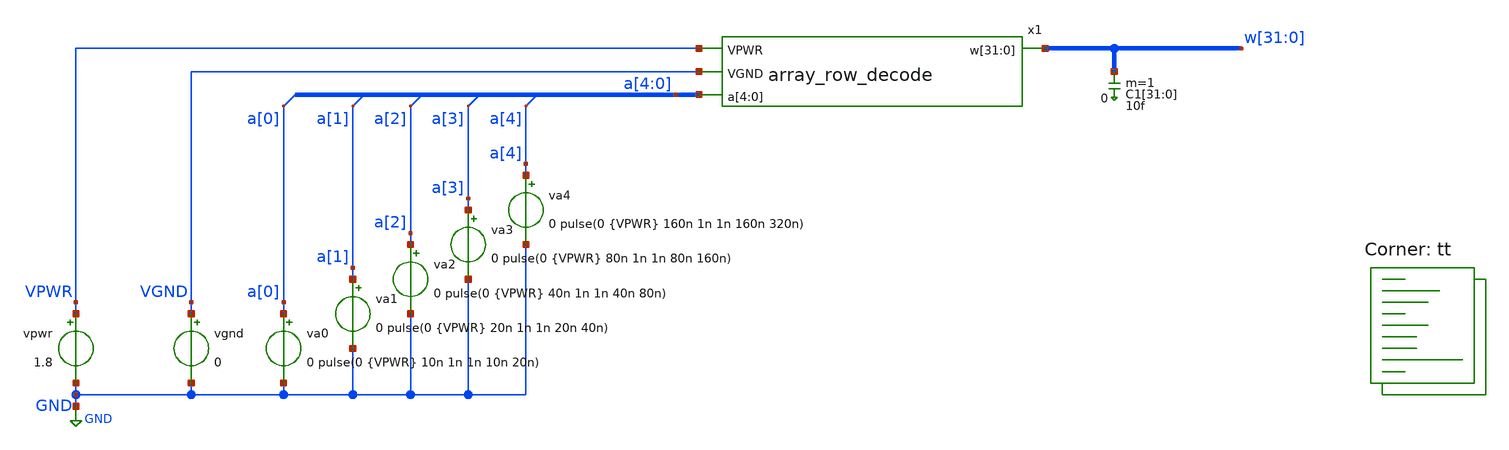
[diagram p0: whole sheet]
** sch_path: xschem/test_array_row_decode.sch
**.subckt test_array_row_decode
x1 VPWR VGND a[4] a[3] a[2] a[1] a[0] w[31] w[30] w[29] w[28] w[27] w[26] w[25] w[24] w[23] w[22]
+ w[21] w[20] w[19] w[18] w[17] w[16] w[15] w[14] w[13] w[12] w[11] w[10] w[9] w[8] w[7] w[6] w[5] w[4]
+ w[3] w[2] w[1] w[0] array_row_decode
vpwr VPWR GND 1.8
va0 a[0] GND 0 pulse(0 {VPWR} 10n 1n 1n 10n 20n)
vgnd VGND GND 0
va1 a[1] GND 0 pulse(0 {VPWR} 20n 1n 1n 20n 40n)
va2 a[2] GND 0 pulse(0 {VPWR} 40n 1n 1n 40n 80n)
va3 a[3] GND 0 pulse(0 {VPWR} 80n 1n 1n 80n 160n)
va4 a[4] GND 0 pulse(0 {VPWR} 160n 1n 1n 160n 320n)
C1[31] w[31] 0 10f m=1
C1[30] w[30] 0 10f m=1
C1[29] w[29] 0 10f m=1
C1[28] w[28] 0 10f m=1
C1[27] w[27] 0 10f m=1
C1[26] w[26] 0 10f m=1
C1[25] w[25] 0 10f m=1
C1[24] w[24] 0 10f m=1
C1[23] w[23] 0 10f m=1
C1[22] w[22] 0 10f m=1
C1[21] w[21] 0 10f m=1
C1[20] w[20] 0 10f m=1
C1[19] w[19] 0 10f m=1
C1[18] w[18] 0 10f m=1
C1[17] w[17] 0 10f m=1
C1[16] w[16] 0 10f m=1
C1[15] w[15] 0 10f m=1
C1[14] w[14] 0 10f m=1
C1[13] w[13] 0 10f m=1
C1[12] w[12] 0 10f m=1
C1[11] w[11] 0 10f m=1
C1[10] w[10] 0 10f m=1
C1[9] w[9] 0 10f m=1
C1[8] w[8] 0 10f m=1
C1[7] w[7] 0 10f m=1
C1[6] w[6] 0 10f m=1
C1[5] w[5] 0 10f m=1
C1[4] w[4] 0 10f m=1
C1[3] w[3] 0 10f m=1
C1[2] w[2] 0 10f m=1
C1[1] w[1] 0 10f m=1
C1[0] w[0] 0 10f m=1
**** begin user architecture code
.lib $::SKYWATER_MODELS/sky130.lib.spice tt



.param VPWR=1.8
.param VSS=0
.options savecurrents
.control
  save all
  op
  remzerovec
  write test_array_row_decode.raw
  set appendwrite
  * tran
  tran 1n 1u
  remzerovec
  write test_array_row_decode.raw
.endc



**** end user architecture code
**.ends

* expanding   symbol:  array_row_decode.sym # of pins=4
** sym_path: xschem/array_row_decode.sym
** sch_path: xschem/array_row_decode.sch
.subckt array_row_decode VPWR VGND a[4] a[3] a[2] a[1] a[0] w[31] w[30] w[29] w[28] w[27] w[26]
+ w[25] w[24] w[23] w[22] w[21] w[20] w[19] w[18] w[17] w[16] w[15] w[14] w[13] w[12] w[11] w[10] w[9] w[8]
+ w[7] w[6] w[5] w[4] w[3] w[2] w[1] w[0]
*.ipin a[4],a[3],a[2],a[1],a[0]
*.ipin VPWR
*.ipin VGND
*.opin
*+ w[31],w[30],w[29],w[28],w[27],w[26],w[25],w[24],w[23],w[22],w[21],w[20],w[19],w[18],w[17],w[16],w[15],w[14],w[13],w[12],w[11],w[10],w[9],w[8],w[7],w[6],w[5],w[4],w[3],w[2],w[1],w[0]
x1 a[4] VGND VGND VPWR VPWR a[4]_b sky130_fd_sc_hd__inv_1
x2 a[3] VGND VGND VPWR VPWR a[3]_b sky130_fd_sc_hd__inv_1
x3 a[2] VGND VGND VPWR VPWR a[2]_b sky130_fd_sc_hd__inv_1
x4 a[1] VGND VGND VPWR VPWR a[1]_b sky130_fd_sc_hd__inv_1
x5 a[0] VGND VGND VPWR VPWR a[0]_b sky130_fd_sc_hd__inv_1
x13 a[2] a[3] VGND VGND VPWR VPWR net8 sky130_fd_sc_hd__nand2_2
x6 a[0]_b a[1]_b VGND VGND VPWR VPWR net1 sky130_fd_sc_hd__nand2_2
x7 a[0] a[1]_b VGND VGND VPWR VPWR net3 sky130_fd_sc_hd__nand2_2
x8 a[0]_b a[1] VGND VGND VPWR VPWR net4 sky130_fd_sc_hd__nand2_2
x9 a[0] a[1] VGND VGND VPWR VPWR net5 sky130_fd_sc_hd__nand2_2
x10 a[2]_b a[3]_b VGND VGND VPWR VPWR net2 sky130_fd_sc_hd__nand2_2
x11 a[2] a[3]_b VGND VGND VPWR VPWR net6 sky130_fd_sc_hd__nand2_2
x12 a[2]_b a[3] VGND VGND VPWR VPWR net7 sky130_fd_sc_hd__nand2_2
x14 net1 net2 a[4] VGND VGND VPWR VPWR w[0] sky130_fd_sc_hd__nor3_1
x15 net3 net2 a[4] VGND VGND VPWR VPWR w[1] sky130_fd_sc_hd__nor3_1
x16 net4 net2 a[4] VGND VGND VPWR VPWR w[2] sky130_fd_sc_hd__nor3_1
x17 net5 net2 a[4] VGND VGND VPWR VPWR w[3] sky130_fd_sc_hd__nor3_1
x18 net1 net6 a[4] VGND VGND VPWR VPWR w[4] sky130_fd_sc_hd__nor3_1
x19 net3 net6 a[4] VGND VGND VPWR VPWR w[5] sky130_fd_sc_hd__nor3_1
x20 net4 net6 a[4] VGND VGND VPWR VPWR w[6] sky130_fd_sc_hd__nor3_1
x21 net5 net6 a[4] VGND VGND VPWR VPWR w[7] sky130_fd_sc_hd__nor3_1
x22 net1 net7 a[4] VGND VGND VPWR VPWR w[8] sky130_fd_sc_hd__nor3_1
x23 net3 net7 a[4] VGND VGND VPWR VPWR w[9] sky130_fd_sc_hd__nor3_1
x24 net4 net7 a[4] VGND VGND VPWR VPWR w[10] sky130_fd_sc_hd__nor3_1
x25 net5 net7 a[4] VGND VGND VPWR VPWR w[11] sky130_fd_sc_hd__nor3_1
x26 net1 net8 a[4] VGND VGND VPWR VPWR w[12] sky130_fd_sc_hd__nor3_1
x27 net3 net8 a[4] VGND VGND VPWR VPWR w[13] sky130_fd_sc_hd__nor3_1
x28 net4 net8 a[4] VGND VGND VPWR VPWR w[14] sky130_fd_sc_hd__nor3_1
x29 net5 net8 a[4] VGND VGND VPWR VPWR w[15] sky130_fd_sc_hd__nor3_1
x30 net1 net2 a[4]_b VGND VGND VPWR VPWR w[16] sky130_fd_sc_hd__nor3_1
x31 net3 net2 a[4]_b VGND VGND VPWR VPWR w[17] sky130_fd_sc_hd__nor3_1
x32 net4 net2 a[4]_b VGND VGND VPWR VPWR w[18] sky130_fd_sc_hd__nor3_1
x33 net5 net2 a[4]_b VGND VGND VPWR VPWR w[19] sky130_fd_sc_hd__nor3_1
x34 net1 net6 a[4]_b VGND VGND VPWR VPWR w[20] sky130_fd_sc_hd__nor3_1
x35 net3 net6 a[4]_b VGND VGND VPWR VPWR w[21] sky130_fd_sc_hd__nor3_1
x36 net4 net6 a[4]_b VGND VGND VPWR VPWR w[22] sky130_fd_sc_hd__nor3_1
x37 net5 net6 a[4]_b VGND VGND VPWR VPWR w[23] sky130_fd_sc_hd__nor3_1
x38 net1 net7 a[4]_b VGND VGND VPWR VPWR w[24] sky130_fd_sc_hd__nor3_1
x39 net3 net7 a[4]_b VGND VGND VPWR VPWR w[25] sky130_fd_sc_hd__nor3_1
x40 net4 net7 a[4]_b VGND VGND VPWR VPWR w[26] sky130_fd_sc_hd__nor3_1
x41 net5 net7 a[4]_b VGND VGND VPWR VPWR w[27] sky130_fd_sc_hd__nor3_1
x42 net1 net8 a[4]_b VGND VGND VPWR VPWR w[28] sky130_fd_sc_hd__nor3_1
x43 net3 net8 a[4]_b VGND VGND VPWR VPWR w[29] sky130_fd_sc_hd__nor3_1
x44 net4 net8 a[4]_b VGND VGND VPWR VPWR w[30] sky130_fd_sc_hd__nor3_1
x45 net5 net8 a[4]_b VGND VGND VPWR VPWR w[31] sky130_fd_sc_hd__nor3_1
x46 VGND VPWR sky130_fd_sc_hd__tapvpwrvgnd_1
x47 VGND VGND VPWR VPWR sky130_fd_sc_hd__decap_3
x48 VGND VPWR sky130_fd_sc_hd__tapvpwrvgnd_1
x49 VGND VPWR sky130_fd_sc_hd__tapvpwrvgnd_1
x50 VGND VGND VPWR VPWR sky130_fd_sc_hd__decap_3
x51 VGND VPWR sky130_fd_sc_hd__tapvpwrvgnd_1
x52 VGND VPWR sky130_fd_sc_hd__tapvpwrvgnd_1
x53 VGND VGND VPWR VPWR sky130_fd_sc_hd__decap_3
x54 VGND VPWR sky130_fd_sc_hd__tapvpwrvgnd_1
x55 VGND VPWR sky130_fd_sc_hd__tapvpwrvgnd_1
x56 VGND VGND VPWR VPWR sky130_fd_sc_hd__decap_3
x57 VGND VPWR sky130_fd_sc_hd__tapvpwrvgnd_1
x58 VGND VPWR sky130_fd_sc_hd__tapvpwrvgnd_1
x59 VGND VGND VPWR VPWR sky130_fd_sc_hd__decap_3
x60 VGND VPWR sky130_fd_sc_hd__tapvpwrvgnd_1
x61 VGND VPWR sky130_fd_sc_hd__tapvpwrvgnd_1
x62 VGND VGND VPWR VPWR sky130_fd_sc_hd__decap_3
x63 VGND VPWR sky130_fd_sc_hd__tapvpwrvgnd_1
x64 VGND VPWR sky130_fd_sc_hd__tapvpwrvgnd_1
x65 VGND VGND VPWR VPWR sky130_fd_sc_hd__decap_3
x66 VGND VPWR sky130_fd_sc_hd__tapvpwrvgnd_1
x67 VGND VPWR sky130_fd_sc_hd__tapvpwrvgnd_1
x68 VGND VGND VPWR VPWR sky130_fd_sc_hd__decap_3
x69 VGND VPWR sky130_fd_sc_hd__tapvpwrvgnd_1
x70 VGND VPWR sky130_fd_sc_hd__tapvpwrvgnd_1
x71 VGND VGND VPWR VPWR sky130_fd_sc_hd__decap_3
x72 VGND VPWR sky130_fd_sc_hd__tapvpwrvgnd_1
x73 VGND VPWR sky130_fd_sc_hd__tapvpwrvgnd_1
x74 VGND VGND VPWR VPWR sky130_fd_sc_hd__decap_3
x75 VGND VPWR sky130_fd_sc_hd__tapvpwrvgnd_1
x76 VGND VPWR sky130_fd_sc_hd__tapvpwrvgnd_1
x77 VGND VGND VPWR VPWR sky130_fd_sc_hd__decap_3
x78 VGND VPWR sky130_fd_sc_hd__tapvpwrvgnd_1
x79 VGND VPWR sky130_fd_sc_hd__tapvpwrvgnd_1
x80 VGND VGND VPWR VPWR sky130_fd_sc_hd__decap_3
x81 VGND VPWR sky130_fd_sc_hd__tapvpwrvgnd_1
x82 VGND VPWR sky130_fd_sc_hd__tapvpwrvgnd_1
x83 VGND VGND VPWR VPWR sky130_fd_sc_hd__decap_3
x84 VGND VPWR sky130_fd_sc_hd__tapvpwrvgnd_1
x85 VGND VPWR sky130_fd_sc_hd__tapvpwrvgnd_1
x86 VGND VGND VPWR VPWR sky130_fd_sc_hd__decap_3
x87 VGND VPWR sky130_fd_sc_hd__tapvpwrvgnd_1
x88 VGND VPWR sky130_fd_sc_hd__tapvpwrvgnd_1
x89 VGND VGND VPWR VPWR sky130_fd_sc_hd__decap_3
x90 VGND VPWR sky130_fd_sc_hd__tapvpwrvgnd_1
x91 VGND VPWR sky130_fd_sc_hd__tapvpwrvgnd_1
x92 VGND VGND VPWR VPWR sky130_fd_sc_hd__decap_3
x93 VGND VPWR sky130_fd_sc_hd__tapvpwrvgnd_1
x94 VGND VPWR sky130_fd_sc_hd__tapvpwrvgnd_1
x95 VGND VGND VPWR VPWR sky130_fd_sc_hd__decap_3
x96 VGND VPWR sky130_fd_sc_hd__tapvpwrvgnd_1
x97 VGND VPWR sky130_fd_sc_hd__tapvpwrvgnd_1
x98 VGND VGND VPWR VPWR sky130_fd_sc_hd__decap_3
x99 VGND VPWR sky130_fd_sc_hd__tapvpwrvgnd_1
x100 VGND VPWR sky130_fd_sc_hd__tapvpwrvgnd_1
x101 VGND VGND VPWR VPWR sky130_fd_sc_hd__decap_3
x102 VGND VPWR sky130_fd_sc_hd__tapvpwrvgnd_1
x103 VGND VPWR sky130_fd_sc_hd__tapvpwrvgnd_1
x104 VGND VGND VPWR VPWR sky130_fd_sc_hd__decap_3
x105 VGND VPWR sky130_fd_sc_hd__tapvpwrvgnd_1
x106 VGND VPWR sky130_fd_sc_hd__tapvpwrvgnd_1
x107 VGND VGND VPWR VPWR sky130_fd_sc_hd__decap_3
x108 VGND VPWR sky130_fd_sc_hd__tapvpwrvgnd_1
x109 VGND VPWR sky130_fd_sc_hd__tapvpwrvgnd_1
x110 VGND VGND VPWR VPWR sky130_fd_sc_hd__decap_3
x111 VGND VPWR sky130_fd_sc_hd__tapvpwrvgnd_1
x112 VGND VPWR sky130_fd_sc_hd__tapvpwrvgnd_1
x113 VGND VGND VPWR VPWR sky130_fd_sc_hd__decap_3
x114 VGND VPWR sky130_fd_sc_hd__tapvpwrvgnd_1
x115 VGND VPWR sky130_fd_sc_hd__tapvpwrvgnd_1
x116 VGND VGND VPWR VPWR sky130_fd_sc_hd__decap_3
x117 VGND VPWR sky130_fd_sc_hd__tapvpwrvgnd_1
x118 VGND VPWR sky130_fd_sc_hd__tapvpwrvgnd_1
x119 VGND VGND VPWR VPWR sky130_fd_sc_hd__decap_3
x120 VGND VPWR sky130_fd_sc_hd__tapvpwrvgnd_1
x121 VGND VPWR sky130_fd_sc_hd__tapvpwrvgnd_1
x122 VGND VGND VPWR VPWR sky130_fd_sc_hd__decap_3
x123 VGND VPWR sky130_fd_sc_hd__tapvpwrvgnd_1
x124 VGND VPWR sky130_fd_sc_hd__tapvpwrvgnd_1
x125 VGND VGND VPWR VPWR sky130_fd_sc_hd__decap_3
x126 VGND VPWR sky130_fd_sc_hd__tapvpwrvgnd_1
x127 VGND VPWR sky130_fd_sc_hd__tapvpwrvgnd_1
x128 VGND VGND VPWR VPWR sky130_fd_sc_hd__decap_3
x129 VGND VPWR sky130_fd_sc_hd__tapvpwrvgnd_1
x130 VGND VPWR sky130_fd_sc_hd__tapvpwrvgnd_1
x131 VGND VGND VPWR VPWR sky130_fd_sc_hd__decap_3
x132 VGND VPWR sky130_fd_sc_hd__tapvpwrvgnd_1
x133 VGND VPWR sky130_fd_sc_hd__tapvpwrvgnd_1
x134 VGND VGND VPWR VPWR sky130_fd_sc_hd__decap_3
x135 VGND VPWR sky130_fd_sc_hd__tapvpwrvgnd_1
x136 VGND VPWR sky130_fd_sc_hd__tapvpwrvgnd_1
x137 VGND VGND VPWR VPWR sky130_fd_sc_hd__decap_3
x138 VGND VPWR sky130_fd_sc_hd__tapvpwrvgnd_1
x139 VGND VPWR sky130_fd_sc_hd__tapvpwrvgnd_1
x140 VGND VGND VPWR VPWR sky130_fd_sc_hd__decap_3
x141 VGND VPWR sky130_fd_sc_hd__tapvpwrvgnd_1
x142 VGND VPWR sky130_fd_sc_hd__tapvpwrvgnd_1
x143 VGND VGND VPWR VPWR sky130_fd_sc_hd__decap_3
x144 VGND VPWR sky130_fd_sc_hd__tapvpwrvgnd_1
x145 VGND VPWR sky130_fd_sc_hd__tapvpwrvgnd_1
x146 VGND VPWR sky130_fd_sc_hd__tapvpwrvgnd_1
.ends

.GLOBAL GND
.end
